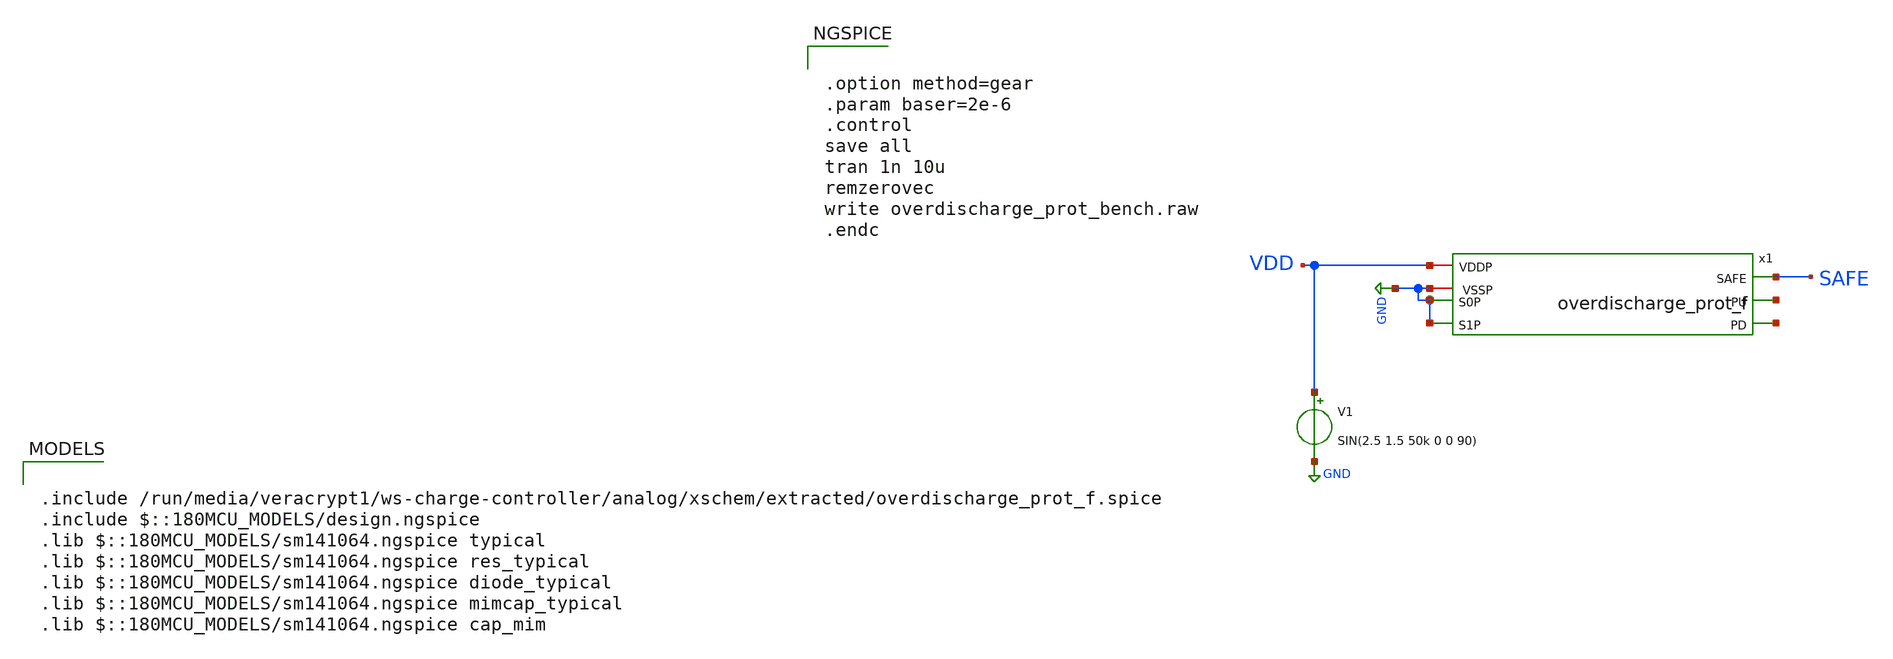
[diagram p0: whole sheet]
** sch_path: analog/xschem/overdischarge_prot_bench.sch
**.subckt overdischarge_prot_bench
V1 VDD GND SIN(2.5 1.5 50k 0 0 90)
x1 VDD GND GND GND SAFE net2 net1 overdischarge_prot_f
**** begin user architecture code


.option method=gear
.param baser=2e-6
.control
save all
tran 1n 10u
remzerovec
write overdischarge_prot_bench.raw
.endc



.include /run/media/veracrypt1/ws-charge-controller/analog/xschem/extracted/overdischarge_prot_f.spice
.include $::180MCU_MODELS/design.ngspice
.lib $::180MCU_MODELS/sm141064.ngspice typical
.lib $::180MCU_MODELS/sm141064.ngspice res_typical
.lib $::180MCU_MODELS/sm141064.ngspice diode_typical
.lib $::180MCU_MODELS/sm141064.ngspice mimcap_typical
.lib $::180MCU_MODELS/sm141064.ngspice cap_mim

**** end user architecture code
**.ends
.GLOBAL GND
.end
